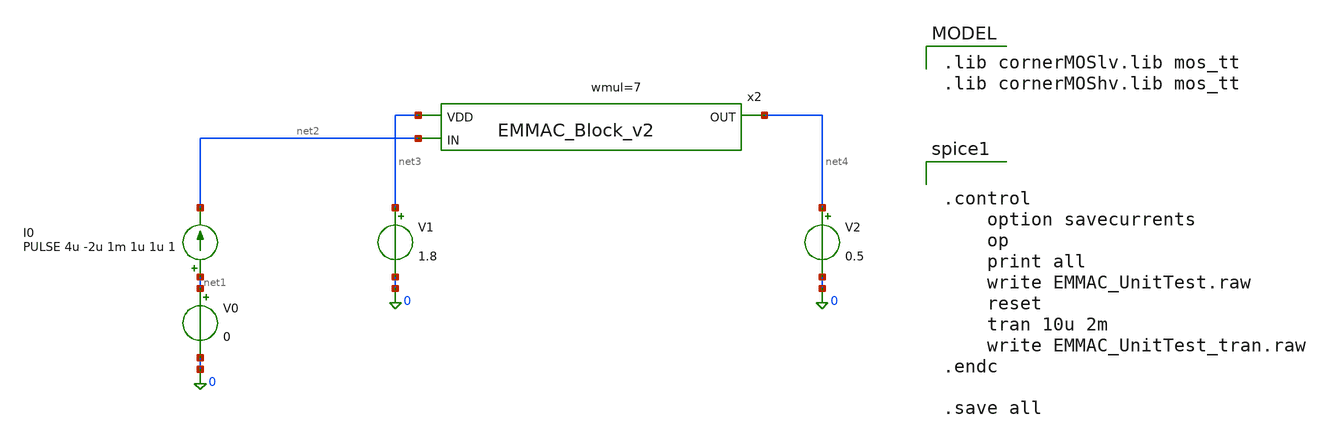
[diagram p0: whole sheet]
** sch_path: src/analog_mac/EMMAC_UnitTest.sch
**.subckt EMMAC_UnitTest
V1 net3 0 1.8
I0 net1 net2 PULSE 4u -2u 1m 1u 1u 1
V2 net4 0 0.5
V0 net1 0 0
x2 net3 net2 net4 EMMAC_Block_v2 wmul=7
**** begin user architecture code
 .lib cornerMOSlv.lib mos_tt
.lib cornerMOShv.lib mos_tt



.control
	option savecurrents
	op
	print all
	write EMMAC_UnitTest.raw
	reset
	tran 10u 2m
	write EMMAC_UnitTest_tran.raw
.endc

.save all


**** end user architecture code
**.ends

* expanding   symbol:  EMMAC_Block_v2.sym # of pins=3
** sym_path: src/analog_mac/EMMAC_Block_v2.sym
** sch_path: src/analog_mac/EMMAC_Block_v2.sch
.subckt EMMAC_Block_v2 VDD IN OUT  wmul=1
*.opin OUT
*.ipin IN
*.ipin VDD
XM1 net5 net3 0 0 sg13_lv_nmos w=1u l=1u ng=1 m=1 mm_ok=1
XM2 net3 net3 0 0 sg13_lv_nmos w=1u l=1u ng=1 m=1 mm_ok=1
XM21 net1 net1 VDD VDD sg13_lv_pmos w=1u l=1u ng=1 m=1 mm_ok=1
XM22 net7 net1 VDD VDD sg13_lv_pmos w=1u l=1u ng=1 m=1 mm_ok=1
XM6 net2 net2 net5 0 sg13_lv_nmos w=1u l=1u ng=1 m=1 mm_ok=1
XM7 net4 net2 net3 0 sg13_lv_nmos w=1u l=1u ng=1 m=1 mm_ok=1
XM3 net8 net6 0 0 sg13_lv_nmos w=1u l=1u ng=1 m=1 mm_ok=1
XM4 net6 net6 0 0 sg13_lv_nmos w=1u l=1u ng=1 m=1 mm_ok=1
XM8 net7 net7 net8 0 sg13_lv_nmos w=1u l=1u ng=1 m=1 mm_ok=1
XM9 net4 net7 net6 0 sg13_lv_nmos w=1u l=1u ng=1 m=1 mm_ok=1
XM23 net4 net4 VDD VDD sg13_lv_pmos w=1u l=0.28u ng=1 m=1 mm_ok=1
XM24 net16 net4 VDD VDD sg13_lv_pmos w=1u l=0.28u ng=1 m=1 mm_ok=1
XM19 net1 net1 IN 0 sg13_hv_nmos w=0.3u l=0.45u ng=1 m=1 mm_ok=1
XM14 IN IN net2 0 sg13_hv_nmos w=0.3u l=0.45u ng=1 m=1 mm_ok=1
XM20 OUT net14 net10 VDD sg13_lv_pmos w=1u l=0.28u ng=1 m=1 mm_ok=1
XM12 net9 net9 0 0 sg13_lv_nmos w=1u l=1u ng=1 m=1 mm_ok=1
XM13 OUT net9 net11 net11 sg13_lv_nmos w=1u l=1u ng=1 m=1 mm_ok=1
XM5 net11 net12 0 0 sg13_lv_nmos w=1u l=1u ng=1 m=1 mm_ok=1
XM25 net10 net12 VDD VDD sg13_lv_pmos w=1u l=0.28u ng=1 m=1 mm_ok=1
XM15 net12 IN 0 0 sg13_lv_nmos w=1u l=1u ng=1 m=1 mm_ok=1
XM17 net12 IN VDD VDD sg13_lv_pmos w=1u l=1u ng=1 m=1 mm_ok=1
XM16 net13 net12 0 0 sg13_lv_nmos w=1u l=1u ng=1 m=1 mm_ok=1
XM18 net13 net12 VDD VDD sg13_lv_pmos w=1u l=1u ng=1 m=1 mm_ok=1
XM28 net14 net14 VDD VDD sg13_lv_pmos w=1u l=0.28u ng=1 m=1 mm_ok=1
XM29 net9 net14 VDD VDD sg13_lv_pmos w=1u l=0.28u ng=1 m=1 mm_ok=1
XM26 net17 net15 0 0 sg13_lv_nmos w=1u l=1u ng=1 m=1 mm_ok=1
XM27 net15 net15 0 0 sg13_lv_nmos w=1u l=1u ng=1 m={wmul} mm_ok=1
XM30 net16 net16 net17 0 sg13_lv_nmos w=1u l=1u ng=1 m=1 mm_ok=1
XM31 net14 net16 net15 0 sg13_lv_nmos w=1u l=1u ng=1 m=1 mm_ok=1
.ends

.end
